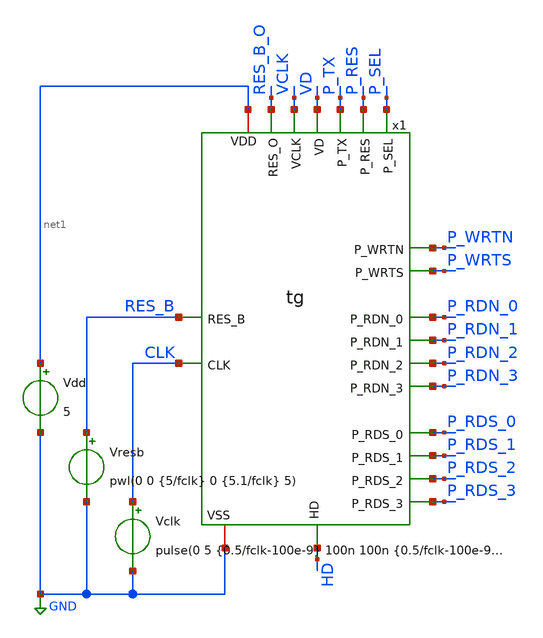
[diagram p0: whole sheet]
** sch_path: member_project/imager/YuMaehashi/design/tb_tg.sch
**.subckt tb_tg
x1 VCLK VD HD P_RDS_3 P_RDS_2 P_RDS_1 P_RDS_0 P_RDN_3 P_RDN_2 P_RDN_1 P_RDN_0 P_WRTS P_WRTN P_TX
+ P_RES P_SEL RES_B_O RES_B CLK net1 GND tg
Vclk CLK GND pulse(0 5 {0.5/fclk-100e-9} 100n 100n {0.5/fclk-100e-9} {1/fclk})
Vresb RES_B GND pwl(0 0 {5/fclk} 0 {5.1/fclk} 5)
Vdd net1 GND 5
**** begin user architecture code
 .include $::LIB/ip62_models


.option savecurrents reltol=1e-4 klu
.temp 40
.param fclk = 1e6

.control
set units=degree
save all

alterparam vthMN = 0 ; Slow:0.1, Fast:-0.1
alterparam vthMP = 0 ; Slow:-0.1, Fast:0.1
reset

tran 512e-9 512e-6
write tb_tg.raw   v(CLK) v(RES_B) v(RES_B_O) v(VD) v(HD) v(VCLK)  v(x1.d1) v(x1.d1_b) v(x1.ffout1)
+  v(x1.d2) v(x1.d2_b) v(x1.ffout2)  v(x1.d4) v(x1.d4_b) v(x1.ffout4)  v(x1.d8) v(x1.d8_b) v(x1.ffout8)
+  v(x1.d16) v(x1.d16_b) v(x1.ffout16)  v(x1.d32) v(x1.d32_b) v(x1.ffout32)  v(x1.d64) v(x1.d64_b) v(x1.ffout64)
+  v(x1.d128_b) v(x1.ffout128)  v(x1.d256_b) v(x1.ffout256)  v(x1.x22.r_b) v(x1.x22.f)  v(P_SEL) v(P_RES) v(P_TX)
+  v(P_WRTN) v(P_WRTS)  v(P_RDN_0) v(P_RDN_1) v(P_RDN_2) v(P_RDN_3)  v(P_RDS_0) v(P_RDS_1) v(P_RDS_2) v(P_RDS_3)
.endc

**** end user architecture code
**.ends
.GLOBAL GND
.end
